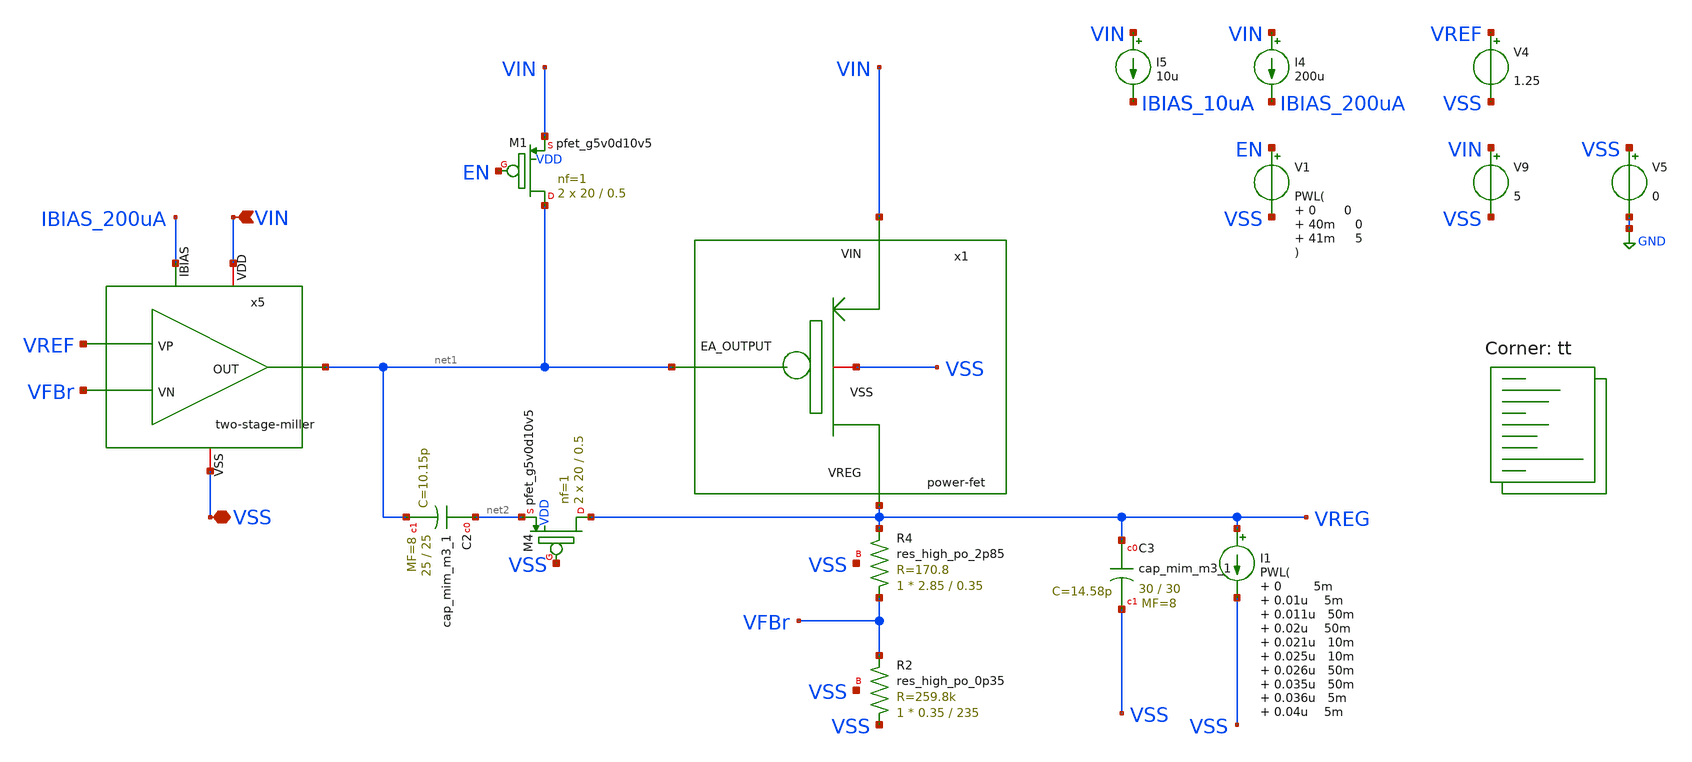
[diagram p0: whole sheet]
** sch_path: bandgap/testbench/tb_tran_startup.sch
**.subckt tb_tran_startup VIN VSS
*.ipin VIN
*.iopin VSS
I4 VIN IBIAS_200uA 200u
V4 VREF VSS 1.25
V5 VSS GND 0
V9 VIN VSS 5
I5 VIN IBIAS_10uA 10u
V1 EN VSS PWL( 0 0 40m 0 41m 5
)
x1 VIN VSS net1 VREG power-fet
XR2 VSS VFBr VSS sky130_fd_pr__res_high_po_0p35 L=235 mult=1 m=1
XR4 VFBr VREG VSS sky130_fd_pr__res_high_po_2p85 L=0.35 mult=1 m=1
x5 VIN net1 VREF VFBr IBIAS_200uA VSS two-stage-miller
XC2 net2 net1 sky130_fd_pr__cap_mim_m3_1 W=25 L=25 MF=8 m=8
XM4 VREG VSS net2 VDD sky130_fd_pr__pfet_g5v0d10v5 L=0.5 W=20 nf=1 ad='int((nf+1)/2) * W/nf * 0.29' as='int((nf+2)/2) * W/nf * 0.29'
+ pd='2*int((nf+1)/2) * (W/nf + 0.29)' ps='2*int((nf+2)/2) * (W/nf + 0.29)' nrd='0.29 / W' nrs='0.29 / W'
+ sa=0 sb=0 sd=0 mult=2 m=2
I1 VREG VSS PWL( 0 5m 0.01u 5m 0.011u 50m 0.02u 50m 0.021u 10m 0.025u 10m 0.026u 50m 0.035u 50m
+ 0.036u 5m 0.04u 5m
)
XC3 VREG VSS sky130_fd_pr__cap_mim_m3_1 W=30 L=30 MF=8 m=8
XM1 net1 EN VIN VDD sky130_fd_pr__pfet_g5v0d10v5 L=0.5 W=20 nf=1 ad='int((nf+1)/2) * W/nf * 0.29' as='int((nf+2)/2) * W/nf * 0.29'
+ pd='2*int((nf+1)/2) * (W/nf + 0.29)' ps='2*int((nf+2)/2) * (W/nf + 0.29)' nrd='0.29 / W' nrs='0.29 / W'
+ sa=0 sb=0 sd=0 mult=2 m=2
**** begin user architecture code



.temp 27
.control

tran 1u 50m

* Nominal output voltage (from regulation region)
let Vout_nom = 1.25
let Vout_95  = 0.95*Vout_nom

* Find Vin where Vout crosses 95%
meas dc Vin_do find v(vin) when v(vreg)=Vout_95

* Measure Vout at that Vin (for completeness)
meas dc Vout_do find v(vreg) when v(vreg)=Vout_95

* Compute dropout voltage
let Vdo = Vin_do - Vout_do

* Compute overshoot, undershoot and peak-to-peak voltage
meas tran Vout_max MAX v(VREGloadtran)
meas tran Vout_min MIN v(VREGloadtran)
let vpp = Vout_max - Vout_min

print Vin_do Vout_do Vdo
print Vout_max Vout_min Vpp
plot VREG EN VIN VREF
plot VREGloadtran2
plot VREG
plot VIN
plot I(load)

.endc


.lib $::SKYWATER_MODELS/sky130.lib.spice tt
**** end user architecture code
**.ends
.GLOBAL GND
.end
